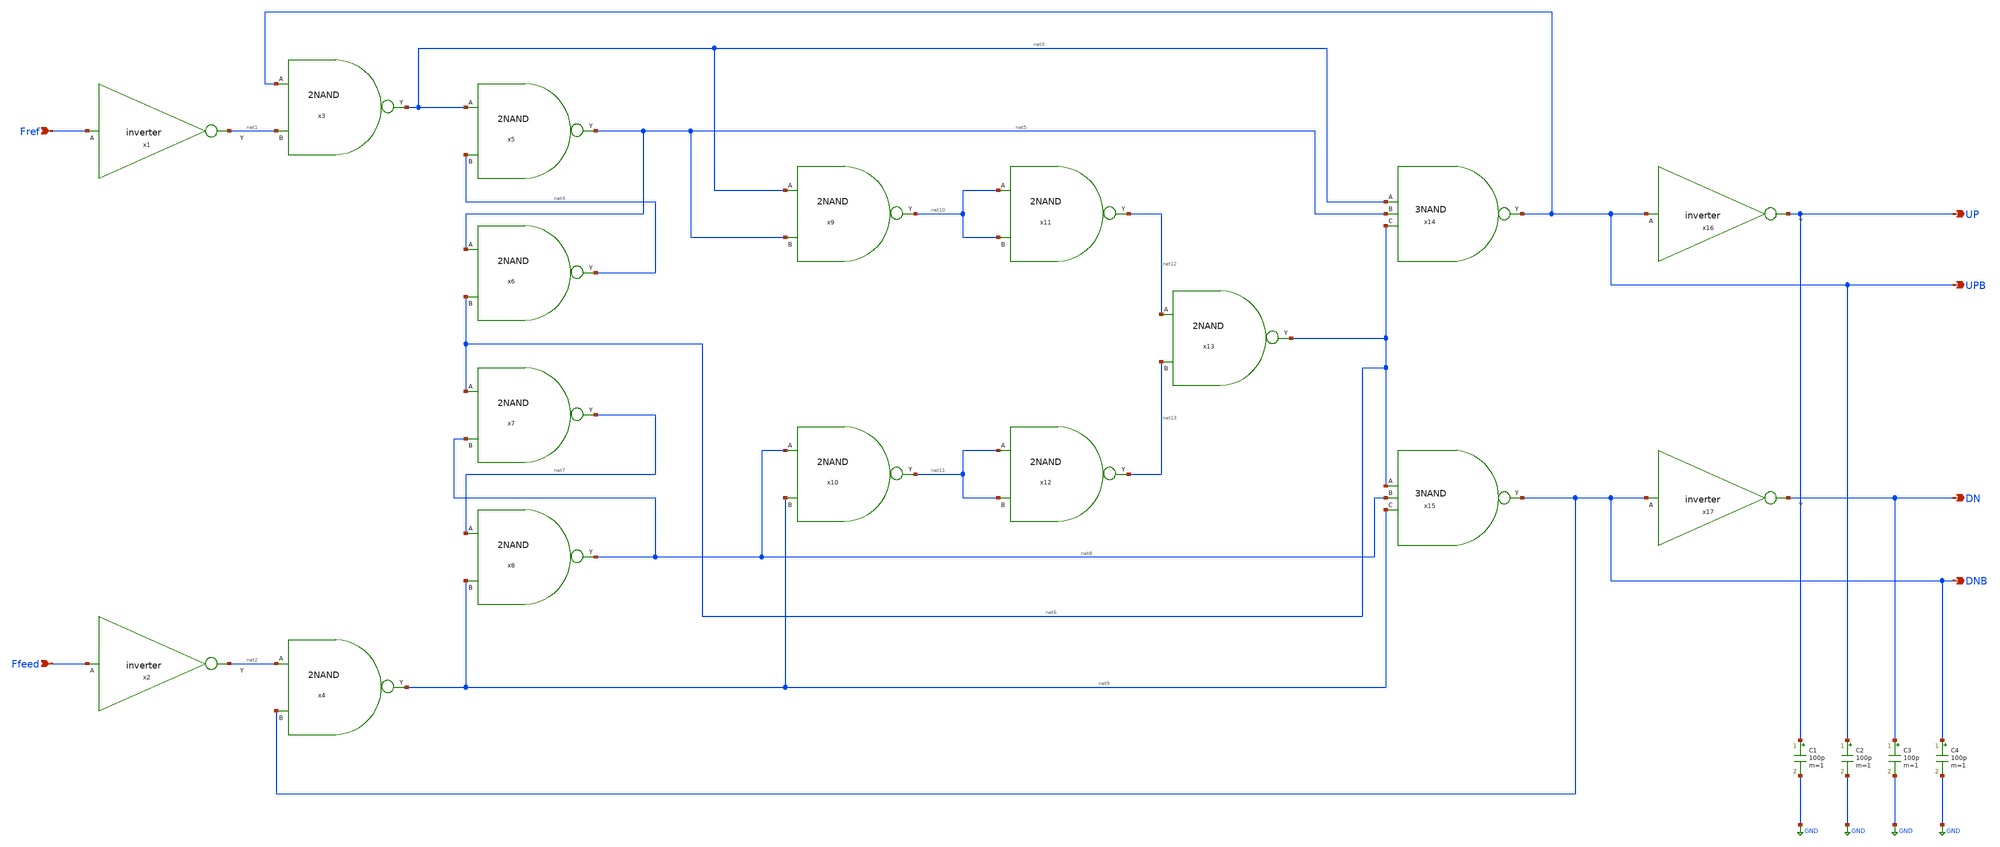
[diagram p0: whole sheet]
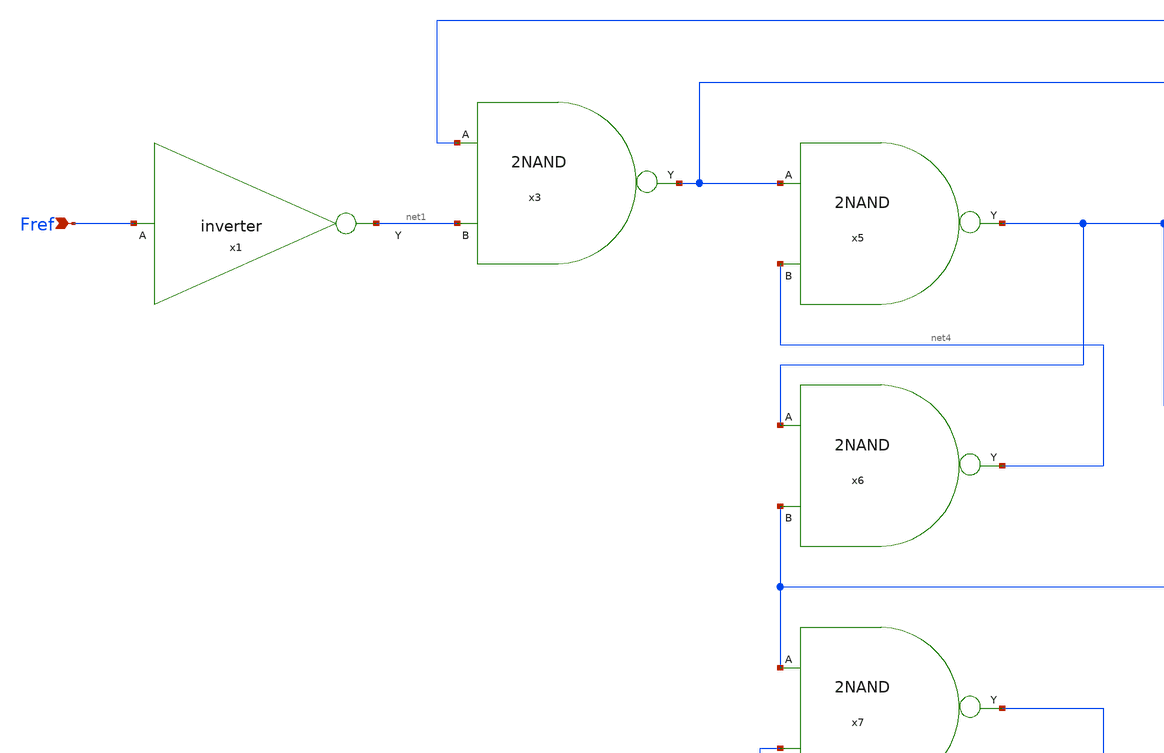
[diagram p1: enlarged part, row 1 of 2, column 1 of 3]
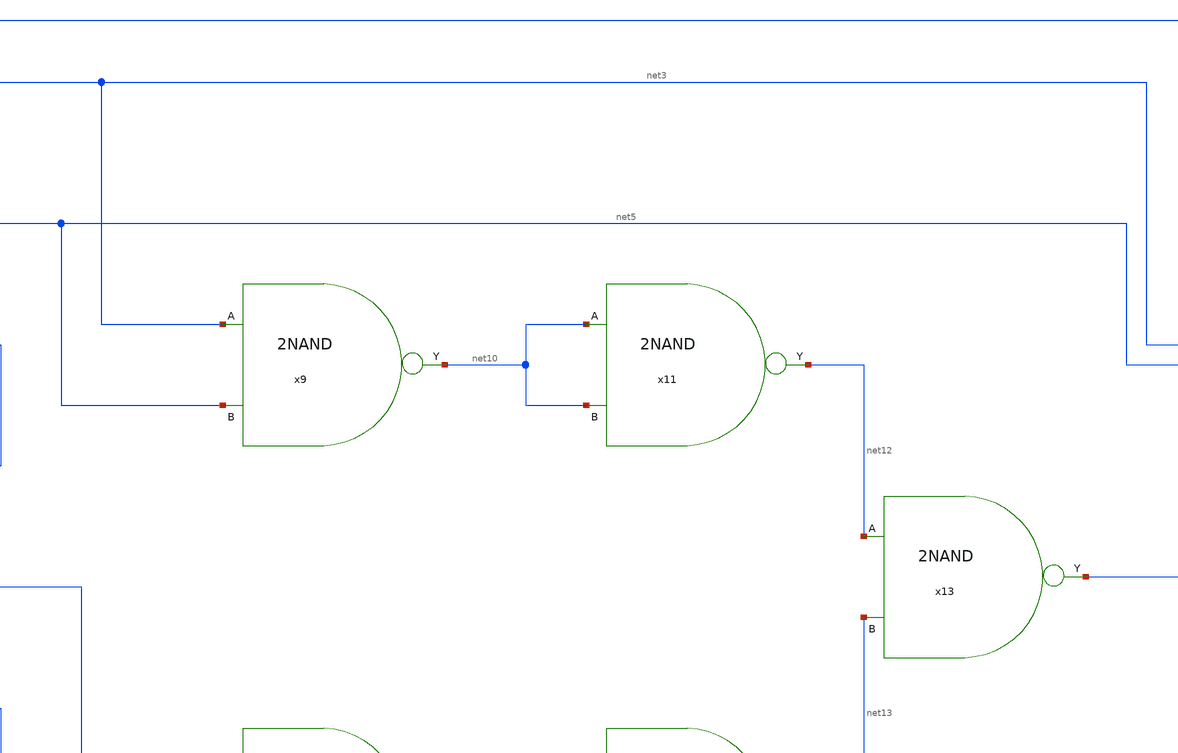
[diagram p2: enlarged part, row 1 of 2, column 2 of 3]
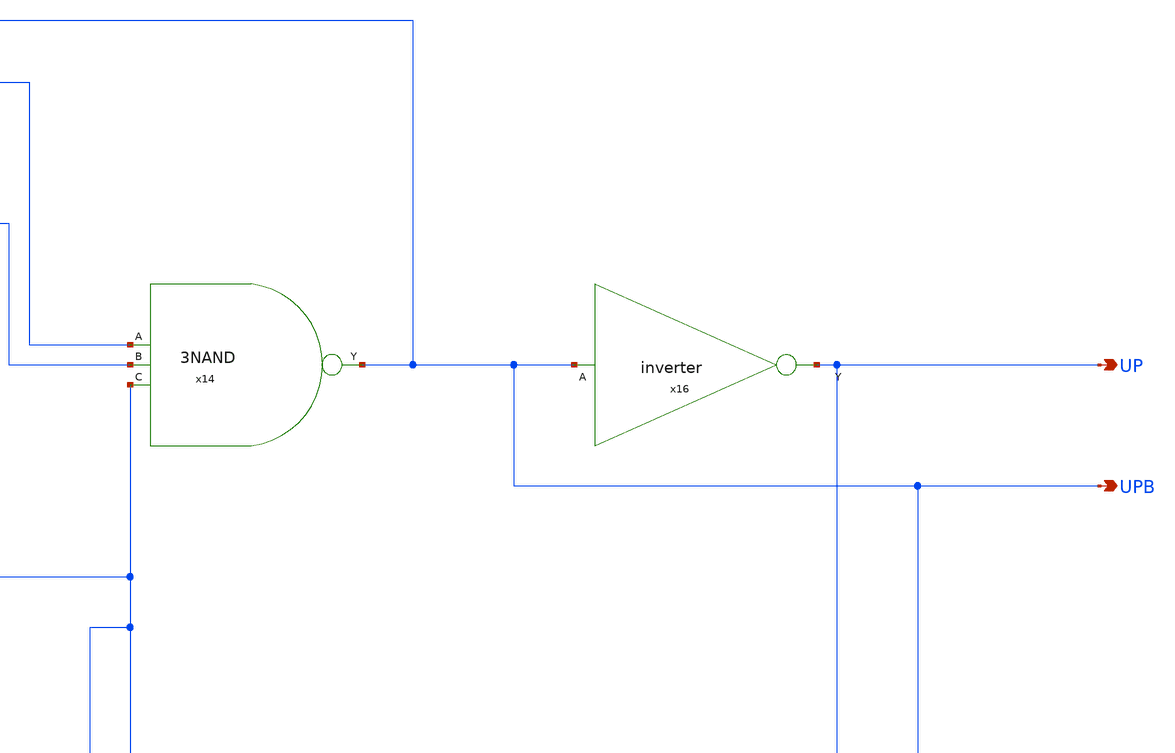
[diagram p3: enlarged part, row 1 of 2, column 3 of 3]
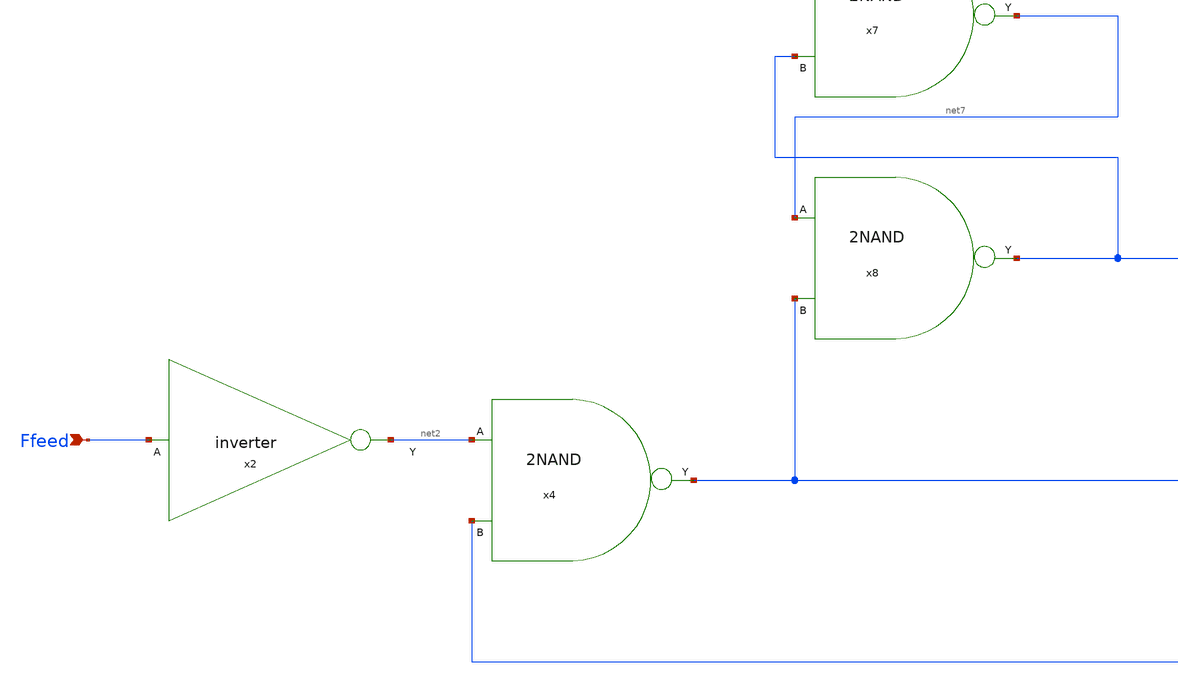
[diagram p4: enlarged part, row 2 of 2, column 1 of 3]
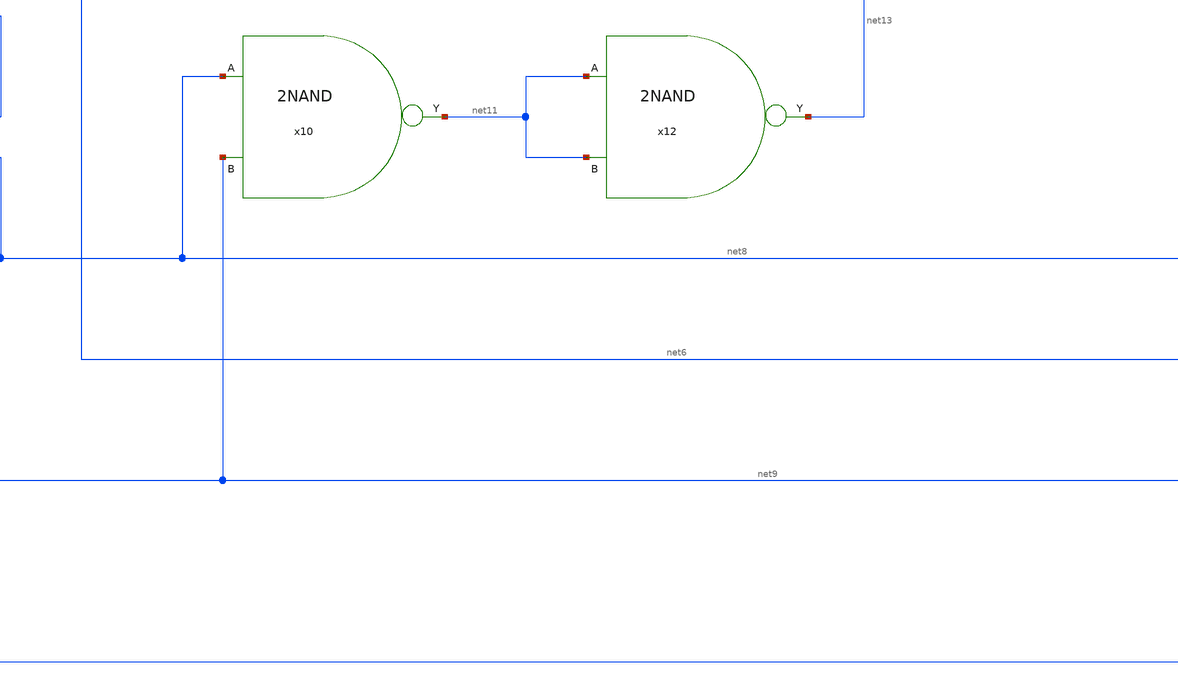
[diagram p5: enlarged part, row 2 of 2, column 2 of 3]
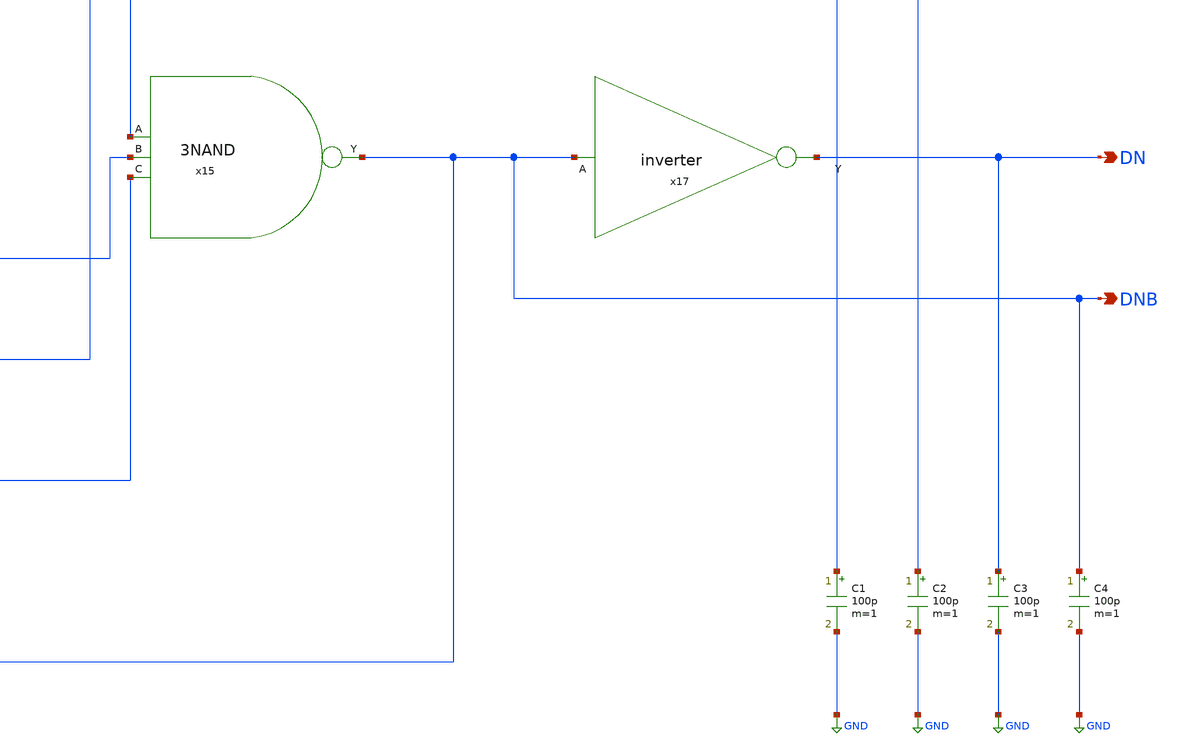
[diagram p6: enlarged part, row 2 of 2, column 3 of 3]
** sch_path: Team 1 Design/design_data/xschem/PFD/PFD.sch
**.subckt PFD Fref Ffeed UP UPB DN DNB
*.ipin Fref
*.ipin Ffeed
*.opin UP
*.opin UPB
*.opin DN
*.opin DNB
x1 net1 Fref inverter
x2 net2 Ffeed inverter
x3 UPB net3 net1 2NAND
x4 net2 net9 DNB 2NAND
x5 net3 net5 net4 2NAND
x6 net5 net4 net6 2NAND
x7 net6 net7 net8 2NAND
x8 net7 net8 net9 2NAND
x9 net3 net10 net5 2NAND
x10 net8 net11 net9 2NAND
x11 net10 net12 net10 2NAND
x12 net11 net13 net11 2NAND
x13 net12 net6 net13 2NAND
x14 UPB net3 net5 net6 3NAND
x15 DNB net6 net8 net9 3NAND
x16 UP UPB inverter
x17 DN DNB inverter
C1 UP GND 100p m=1
C2 UPB GND 100p m=1
C3 DN GND 100p m=1
C4 DNB GND 100p m=1
**.ends
.GLOBAL GND
.end
